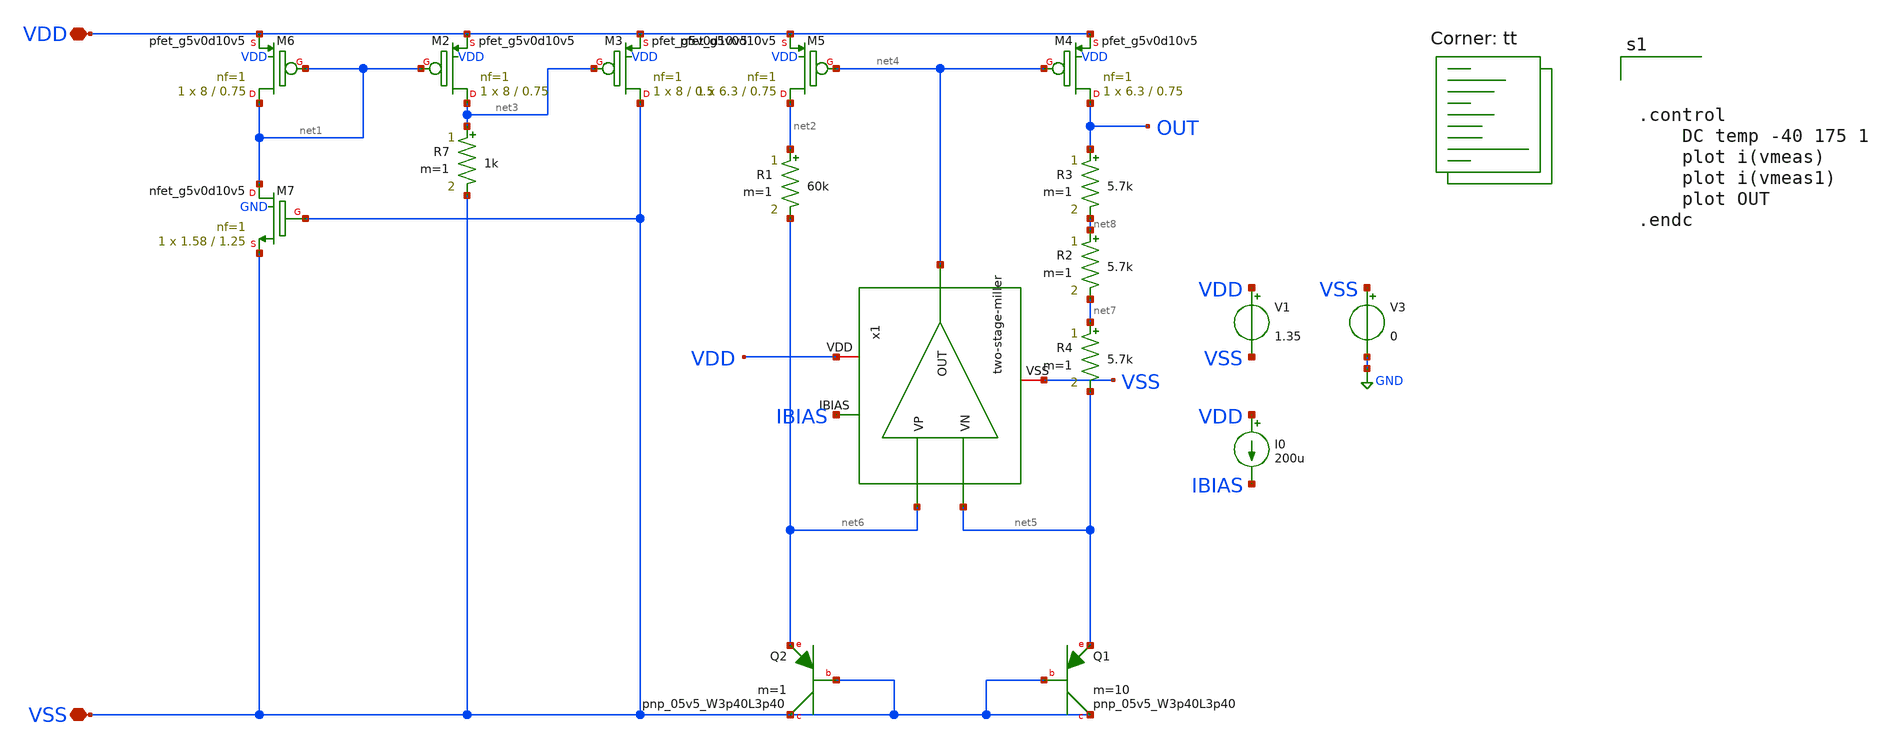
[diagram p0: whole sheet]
** sch_path: bandgap/bandgap_5v/pmos-current-source/bandgap-testing.sch
**.subckt bandgap-testing VDD VSS
*.iopin VDD
*.iopin VSS
XM4 OUT net4 VDD VDD sky130_fd_pr__pfet_g5v0d10v5 L=0.75 W=6.3 nf=1 ad='int((nf+1)/2) * W/nf * 0.29'
+ as='int((nf+2)/2) * W/nf * 0.29' pd='2*int((nf+1)/2) * (W/nf + 0.29)' ps='2*int((nf+2)/2) * (W/nf + 0.29)'
+ nrd='0.29 / W' nrs='0.29 / W' sa=0 sb=0 sd=0 mult=1 m=1
XM5 net2 net4 VDD VDD sky130_fd_pr__pfet_g5v0d10v5 L=0.75 W=6.3 nf=1 ad='int((nf+1)/2) * W/nf * 0.29'
+ as='int((nf+2)/2) * W/nf * 0.29' pd='2*int((nf+1)/2) * (W/nf + 0.29)' ps='2*int((nf+2)/2) * (W/nf + 0.29)'
+ nrd='0.29 / W' nrs='0.29 / W' sa=0 sb=0 sd=0 mult=1 m=1
XM2 net3 net1 VDD VDD sky130_fd_pr__pfet_g5v0d10v5 L=0.75 W=8 nf=1 ad='int((nf+1)/2) * W/nf * 0.29' as='int((nf+2)/2) * W/nf * 0.29'
+ pd='2*int((nf+1)/2) * (W/nf + 0.29)' ps='2*int((nf+2)/2) * (W/nf + 0.29)' nrd='0.29 / W' nrs='0.29 / W'
+ sa=0 sb=0 sd=0 mult=1 m=1
XM3 VSS net3 VDD VDD sky130_fd_pr__pfet_g5v0d10v5 L=0.5 W=8 nf=1 ad='int((nf+1)/2) * W/nf * 0.29' as='int((nf+2)/2) * W/nf * 0.29'
+ pd='2*int((nf+1)/2) * (W/nf + 0.29)' ps='2*int((nf+2)/2) * (W/nf + 0.29)' nrd='0.29 / W' nrs='0.29 / W'
+ sa=0 sb=0 sd=0 mult=1 m=1
XM6 net1 net1 VDD VDD sky130_fd_pr__pfet_g5v0d10v5 L=0.75 W=8 nf=1 ad='int((nf+1)/2) * W/nf * 0.29' as='int((nf+2)/2) * W/nf * 0.29'
+ pd='2*int((nf+1)/2) * (W/nf + 0.29)' ps='2*int((nf+2)/2) * (W/nf + 0.29)' nrd='0.29 / W' nrs='0.29 / W'
+ sa=0 sb=0 sd=0 mult=1 m=1
XM7 net1 VSS VSS GND sky130_fd_pr__nfet_g5v0d10v5 L=1.25 W=1.58 nf=1 ad='int((nf+1)/2) * W/nf * 0.29'
+ as='int((nf+2)/2) * W/nf * 0.29' pd='2*int((nf+1)/2) * (W/nf + 0.29)' ps='2*int((nf+2)/2) * (W/nf + 0.29)'
+ nrd='0.29 / W' nrs='0.29 / W' sa=0 sb=0 sd=0 mult=1 m=1
R1 net2 net6 60k m=1
R3 OUT net8 5.7k m=1
XQ1 VSS VSS net5 sky130_fd_pr__pnp_05v5_W3p40L3p40 m=10
XQ2 VSS VSS net6 sky130_fd_pr__pnp_05v5_W3p40L3p40 m=1
R7 net3 VSS 1k m=1
V1 VDD VSS 1.35
V3 VSS GND 0
x1 VDD net4 net6 net5 IBIAS VSS two-stage-miller
I0 VDD IBIAS 200u
R2 net8 net7 5.7k m=1
R4 net7 net5 5.7k m=1
**** begin user architecture code
.lib $::SKYWATER_MODELS/sky130.lib.spice tt



.control
	DC temp -40 175 1
	plot i(vmeas)
	plot i(vmeas1)
	plot OUT
.endc



**** end user architecture code
**.ends

* expanding   symbol:  icdec-biomedical-pmic/xschem/error-amplifier/schematics/two-stage-miller.sym
*+ # of pins=6
** sym_path: xschem/error-amplifier/schematics/two-stage-miller.sym
** sch_path: xschem/error-amplifier/schematics/two-stage-miller.sch
.subckt two-stage-miller VDD OUT VP VN IBIAS VSS
*.iopin VDD
*.iopin VSS
*.ipin IBIAS
*.ipin VP
*.ipin VN
*.opin OUT
XM1 net3 net2 VDD VDD sky130_fd_pr__pfet_g5v0d10v5 L=1.25 W=75.2 nf=8 ad='int((nf+1)/2) * W/nf * 0.29'
+ as='int((nf+2)/2) * W/nf * 0.29' pd='2*int((nf+1)/2) * (W/nf + 0.29)' ps='2*int((nf+2)/2) * (W/nf + 0.29)'
+ nrd='0.29 / W' nrs='0.29 / W' sa=0 sb=0 sd=0 mult=1 m=1
XM2 net2 net2 VDD VDD sky130_fd_pr__pfet_g5v0d10v5 L=1.25 W=75.2 nf=8 ad='int((nf+1)/2) * W/nf * 0.29'
+ as='int((nf+2)/2) * W/nf * 0.29' pd='2*int((nf+1)/2) * (W/nf + 0.29)' ps='2*int((nf+2)/2) * (W/nf + 0.29)'
+ nrd='0.29 / W' nrs='0.29 / W' sa=0 sb=0 sd=0 mult=1 m=1
XM3 net3 VN net1 VSS sky130_fd_pr__nfet_g5v0d10v5 L=0.5 W=37.7 nf=8 ad='int((nf+1)/2) * W/nf * 0.29'
+ as='int((nf+2)/2) * W/nf * 0.29' pd='2*int((nf+1)/2) * (W/nf + 0.29)' ps='2*int((nf+2)/2) * (W/nf + 0.29)'
+ nrd='0.29 / W' nrs='0.29 / W' sa=0 sb=0 sd=0 mult=1 m=1
XM4 net2 VP net1 VSS sky130_fd_pr__nfet_g5v0d10v5 L=0.5 W=37.7 nf=8 ad='int((nf+1)/2) * W/nf * 0.29'
+ as='int((nf+2)/2) * W/nf * 0.29' pd='2*int((nf+1)/2) * (W/nf + 0.29)' ps='2*int((nf+2)/2) * (W/nf + 0.29)'
+ nrd='0.29 / W' nrs='0.29 / W' sa=0 sb=0 sd=0 mult=1 m=1
XM5 net1 IBIAS VSS VSS sky130_fd_pr__nfet_g5v0d10v5 L=1.25 W=60 nf=8 ad='int((nf+1)/2) * W/nf * 0.29'
+ as='int((nf+2)/2) * W/nf * 0.29' pd='2*int((nf+1)/2) * (W/nf + 0.29)' ps='2*int((nf+2)/2) * (W/nf + 0.29)'
+ nrd='0.29 / W' nrs='0.29 / W' sa=0 sb=0 sd=0 mult=1 m=1
XM6 IBIAS IBIAS VSS VSS sky130_fd_pr__nfet_g5v0d10v5 L=1.25 W=60 nf=8 ad='int((nf+1)/2) * W/nf * 0.29'
+ as='int((nf+2)/2) * W/nf * 0.29' pd='2*int((nf+1)/2) * (W/nf + 0.29)' ps='2*int((nf+2)/2) * (W/nf + 0.29)'
+ nrd='0.29 / W' nrs='0.29 / W' sa=0 sb=0 sd=0 mult=1 m=1
XM7 OUT net3 VDD VDD sky130_fd_pr__pfet_g5v0d10v5 L=1.25 W=160 nf=16 ad='int((nf+1)/2) * W/nf * 0.29'
+ as='int((nf+2)/2) * W/nf * 0.29' pd='2*int((nf+1)/2) * (W/nf + 0.29)' ps='2*int((nf+2)/2) * (W/nf + 0.29)'
+ nrd='0.29 / W' nrs='0.29 / W' sa=0 sb=0 sd=0 mult=1 m=1
XM8 OUT IBIAS VSS VSS sky130_fd_pr__nfet_g5v0d10v5 L=1.25 W=60 nf=8 ad='int((nf+1)/2) * W/nf * 0.29'
+ as='int((nf+2)/2) * W/nf * 0.29' pd='2*int((nf+1)/2) * (W/nf + 0.29)' ps='2*int((nf+2)/2) * (W/nf + 0.29)'
+ nrd='0.29 / W' nrs='0.29 / W' sa=0 sb=0 sd=0 mult=1 m=1
XC1 net4 net3 sky130_fd_pr__cap_mim_m3_1 W=25 L=25 MF=8 m=8
XM9 OUT VSS net4 VDD sky130_fd_pr__pfet_g5v0d10v5 L=0.9 W=20 nf=4 ad='int((nf+1)/2) * W/nf * 0.29' as='int((nf+2)/2) * W/nf * 0.29'
+ pd='2*int((nf+1)/2) * (W/nf + 0.29)' ps='2*int((nf+2)/2) * (W/nf + 0.29)' nrd='0.29 / W' nrs='0.29 / W'
+ sa=0 sb=0 sd=0 mult=1 m=1
.ends

.GLOBAL GND
.end
